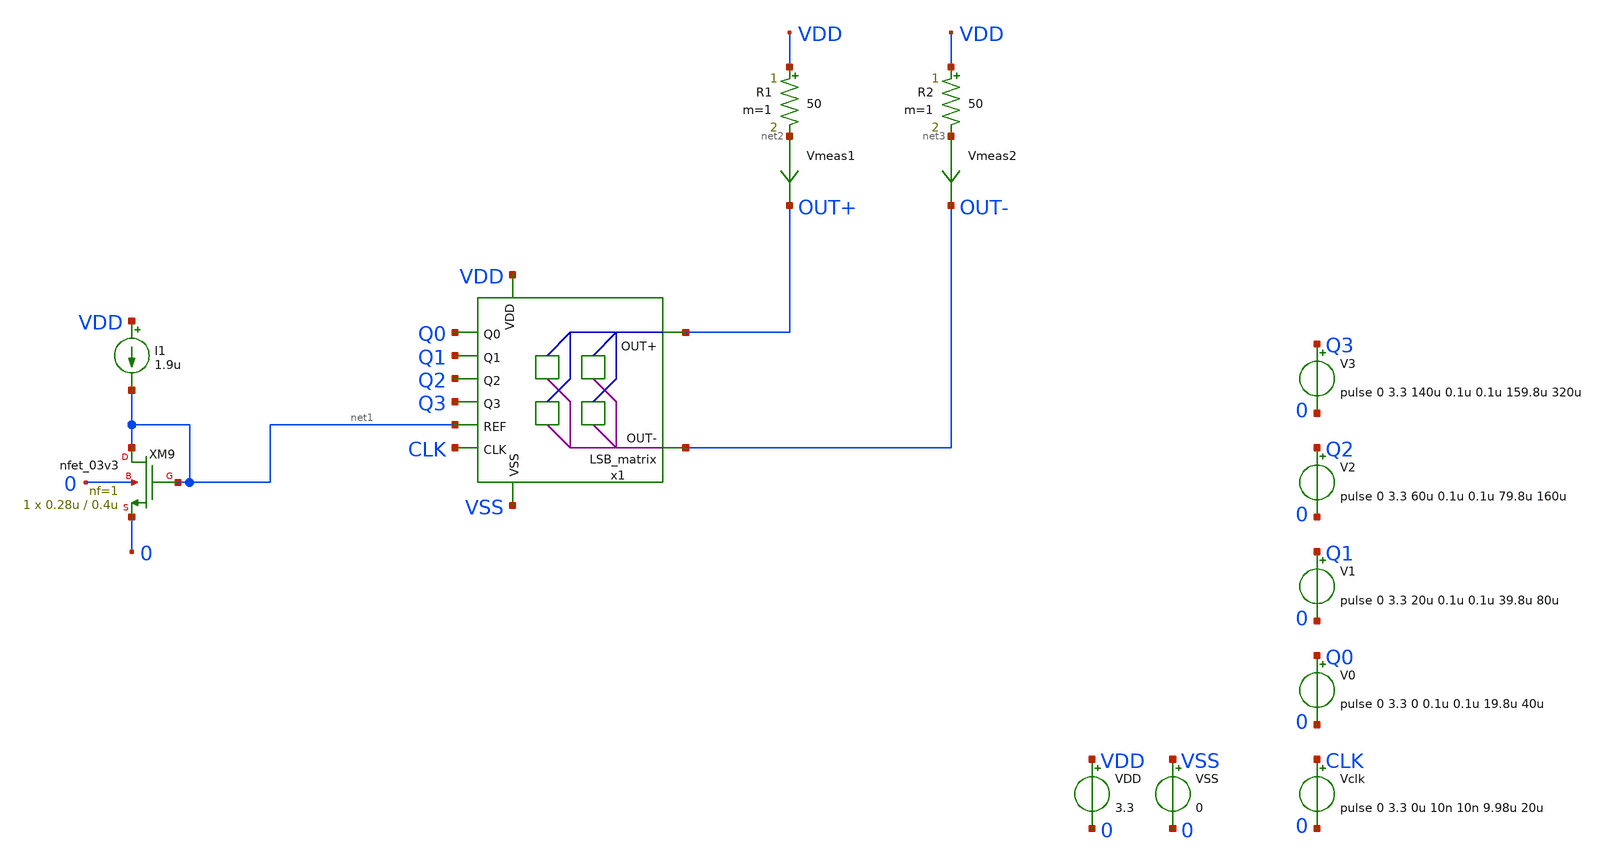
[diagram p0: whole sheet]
** sch_path: DAC/xschem/analog_cell/test/test)LSB_matrix.sch
**.subckt test)LSB_matrix
R1 VDD net2 50 m=1
R2 VDD net3 50 m=1
Vmeas1 net2 OUT+ 0
.save i(vmeas1)
Vmeas2 net3 OUT- 0
.save i(vmeas2)
VDD VDD 0 3.3
VSS VSS 0 0
V2 Q2 0 pulse 0 3.3 60u 0.1u 0.1u 79.8u 160u
V1 Q1 0 pulse 0 3.3 20u 0.1u 0.1u 39.8u 80u
V0 Q0 0 pulse 0 3.3 0 0.1u 0.1u 19.8u 40u
Vclk CLK 0 pulse 0 3.3 0u 10n 10n 9.98u 20u
V3 Q3 0 pulse 0 3.3 140u 0.1u 0.1u 159.8u 320u
x1 VDD Q0 OUT+ Q1 OUT- Q2 Q3 net1 CLK VSS LSB_matrix
I1 VDD net1 1.9u
XM9 net1 net1 0 0 nfet_03v3 L=0.4u W=0.28u nf=1 ad='int((nf+1)/2) * W/nf * 0.18u' as='int((nf+2)/2) * W/nf * 0.18u'
+ pd='2*int((nf+1)/2) * (W/nf + 0.18u)' ps='2*int((nf+2)/2) * (W/nf + 0.18u)' nrd='0.18u / W' nrs='0.18u / W'
+ sa=0 sb=0 sd=0 m=1
**** begin user architecture code



.options savecurrents

.control
	tran 1u 320u
	plot v(CLK)
	plot i(Vmeas1) i(Vmeas2)
	plot v(Q0)
	plot v(Q1)
	plot v(Q2)
	plot v(Q3)

.endc

.save all



.include $::180MCU_MODELS/design.ngspice
.lib $::180MCU_MODELS/sm141064.ngspice typical
.lib $::180MCU_MODELS/sm141064.ngspice res_typical
.lib $::180MCU_MODELS/sm141064.ngspice moscap_typical
.include $::180MCU_REF_7T5V0/spice/gf180mcu_fd_sc_mcu7t5v0.spice
*.lib $::180MCU_MODELS/sm141064.ngspice res_statistical

**** end user architecture code
**.ends
.end
